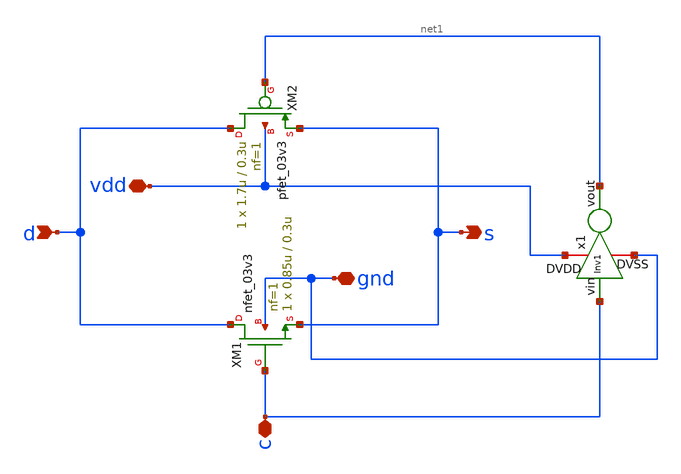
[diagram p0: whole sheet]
** sch_path: src/schematic/TG/transgate.sch
**.subckt transgate gnd vdd c d s
*.iopin gnd
*.iopin vdd
*.iopin c
*.ipin d
*.opin s
XM1 d c s gnd nfet_03v3 L=0.3u W=0.85u nf=1 ad='int((nf+1)/2) * W/nf * 0.18u' as='int((nf+2)/2) * W/nf * 0.18u'
+ pd='2*int((nf+1)/2) * (W/nf + 0.18u)' ps='2*int((nf+2)/2) * (W/nf + 0.18u)' nrd='0.18u / W' nrs='0.18u / W'
+ sa=0 sb=0 sd=0 m=1
XM2 d net1 s vdd pfet_03v3 L=0.3u W=1.7u nf=1 ad='int((nf+1)/2) * W/nf * 0.18u' as='int((nf+2)/2) * W/nf * 0.18u'
+ pd='2*int((nf+1)/2) * (W/nf + 0.18u)' ps='2*int((nf+2)/2) * (W/nf + 0.18u)' nrd='0.18u / W' nrs='0.18u / W'
+ sa=0 sb=0 sd=0 m=1
x1 vdd c net1 gnd Inv1
**.ends

* expanding   symbol:  src/schematic/INV/Inv1.sym # of pins=4
** sym_path: src/schematic/INV/Inv1.sym
** sch_path: src/schematic/INV/Inv1.sch
.subckt Inv1 DVDD vin vout DVSS
*.ipin vin
*.opin vout
*.iopin DVDD
*.iopin DVSS
XM3 vout vin DVDD DVDD pfet_03v3 L=0.3u W=1.7u nf=1 ad='int((nf+1)/2) * W/nf * 0.18u' as='int((nf+2)/2) * W/nf * 0.18u'
+ pd='2*int((nf+1)/2) * (W/nf + 0.18u)' ps='2*int((nf+2)/2) * (W/nf + 0.18u)' nrd='0.18u / W' nrs='0.18u / W'
+ sa=0 sb=0 sd=0 m=1
XM4 vout vin DVSS DVSS nfet_03v3 L=0.3u W=0.85u nf=1 ad='int((nf+1)/2) * W/nf * 0.18u' as='int((nf+2)/2) * W/nf * 0.18u'
+ pd='2*int((nf+1)/2) * (W/nf + 0.18u)' ps='2*int((nf+2)/2) * (W/nf + 0.18u)' nrd='0.18u / W' nrs='0.18u / W'
+ sa=0 sb=0 sd=0 m=1
.ends

.end
